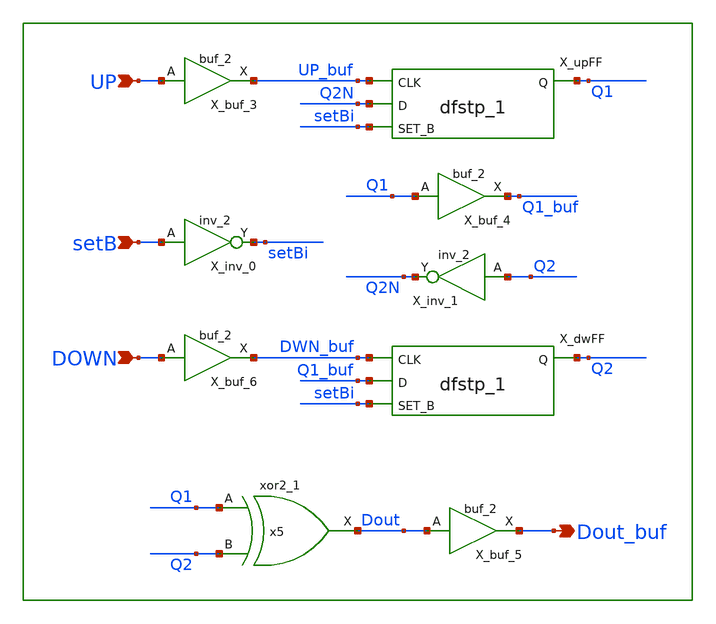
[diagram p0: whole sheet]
** sch_path: xschem/lib/DLib_UpDownCounter.sch
**.subckt DLib_UpDownCounter DOWN Dout_buf UP setB
*.ipin DOWN
*.opin Dout_buf
*.ipin UP
*.ipin setB
X_inv_0 setB VGND VNB VPB VPWR setBi sky130_fd_sc_hd__inv_2
X_upFF UP_buf Q2N setBi VGND VNB VPB VPWR Q1 sky130_fd_sc_hd__dfstp_1
X_dwFF DWN_buf Q1_buf setBi VGND VNB VPB VPWR Q2 sky130_fd_sc_hd__dfstp_1
x5 Q1 Q2 VGND VNB VPB VPWR Dout sky130_fd_sc_hd__xor2_1
X_buf_3 UP VGND VNB VPB VPWR UP_buf sky130_fd_sc_hd__buf_2
X_buf_4 Q1 VGND VNB VPB VPWR Q1_buf sky130_fd_sc_hd__buf_2
X_buf_5 Dout VGND VNB VPB VPWR Dout_buf sky130_fd_sc_hd__buf_2
X_buf_6 DOWN VGND VNB VPB VPWR DWN_buf sky130_fd_sc_hd__buf_2
X_inv_1 Q2 VGND VNB VPB VPWR Q2N sky130_fd_sc_hd__inv_2
**.ends
.end
